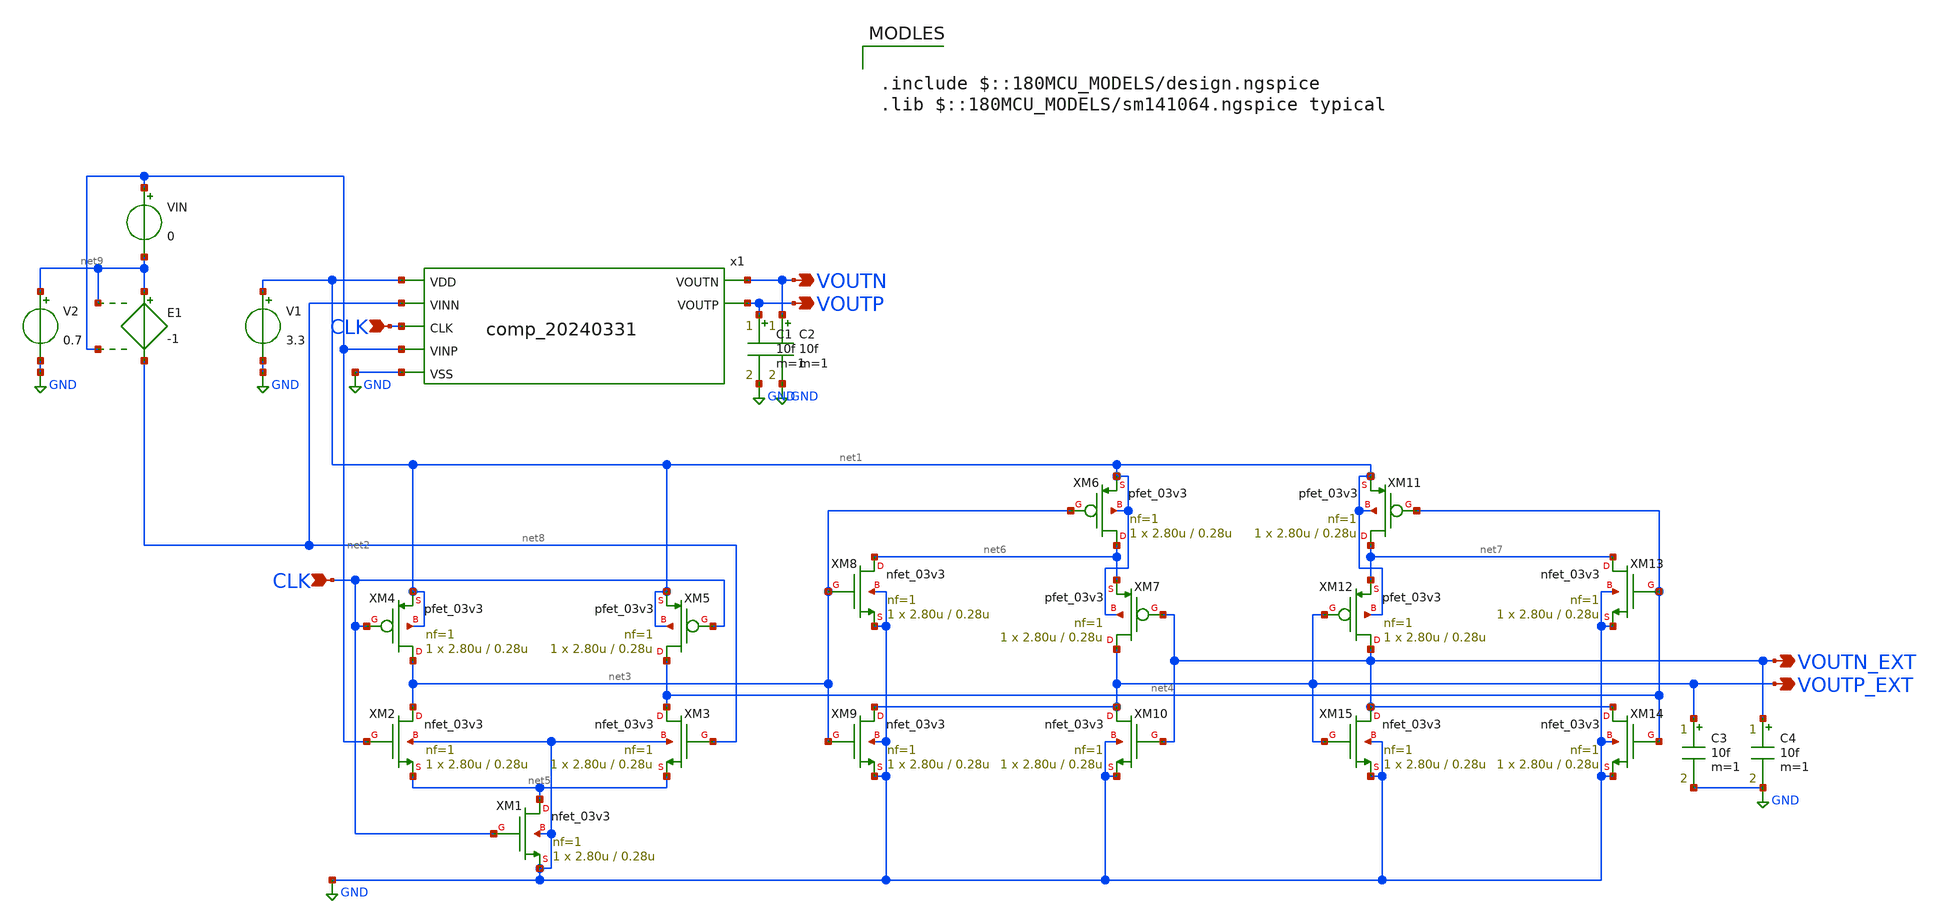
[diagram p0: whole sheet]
** sch_path: review/0407/comp_20240331/tb/tb_like_p78.sch
**.subckt tb_like_p78 CLK VOUTN VOUTP CLK VOUTP_EXT VOUTN_EXT
*.ipin CLK
*.opin VOUTN
*.opin VOUTP
*.ipin CLK
*.opin VOUTP_EXT
*.opin VOUTN_EXT
V1 net1 GND 3.3
V2 net9 GND 0.7
XM1 net5 CLK GND GND nfet_03v3 L=0.28u W=2.80u nf=1 ad='int((nf+1)/2) * W/nf * 0.18u' as='int((nf+2)/2) * W/nf * 0.18u'
+ pd='2*int((nf+1)/2) * (W/nf + 0.18u)' ps='2*int((nf+2)/2) * (W/nf + 0.18u)' nrd='0.18u / W' nrs='0.18u / W'
+ sa=0 sb=0 sd=0 m=1
XM2 net3 net2 net5 GND nfet_03v3 L=0.28u W=2.80u nf=1 ad='int((nf+1)/2) * W/nf * 0.18u' as='int((nf+2)/2) * W/nf * 0.18u'
+ pd='2*int((nf+1)/2) * (W/nf + 0.18u)' ps='2*int((nf+2)/2) * (W/nf + 0.18u)' nrd='0.18u / W' nrs='0.18u / W'
+ sa=0 sb=0 sd=0 m=1
XM4 net3 CLK net1 net1 pfet_03v3 L=0.28u W=2.80u nf=1 ad='int((nf+1)/2) * W/nf * 0.18u' as='int((nf+2)/2) * W/nf * 0.18u'
+ pd='2*int((nf+1)/2) * (W/nf + 0.18u)' ps='2*int((nf+2)/2) * (W/nf + 0.18u)' nrd='0.18u / W' nrs='0.18u / W'
+ sa=0 sb=0 sd=0 m=1
XM6 net6 net3 net1 net1 pfet_03v3 L=0.28u W=2.80u nf=1 ad='int((nf+1)/2) * W/nf * 0.18u' as='int((nf+2)/2) * W/nf * 0.18u'
+ pd='2*int((nf+1)/2) * (W/nf + 0.18u)' ps='2*int((nf+2)/2) * (W/nf + 0.18u)' nrd='0.18u / W' nrs='0.18u / W'
+ sa=0 sb=0 sd=0 m=1
XM7 VOUTP_EXT VOUTN_EXT net6 net1 pfet_03v3 L=0.28u W=2.80u nf=1 ad='int((nf+1)/2) * W/nf * 0.18u' as='int((nf+2)/2) * W/nf * 0.18u'
+ pd='2*int((nf+1)/2) * (W/nf + 0.18u)' ps='2*int((nf+2)/2) * (W/nf + 0.18u)' nrd='0.18u / W' nrs='0.18u / W'
+ sa=0 sb=0 sd=0 m=1
XM8 net6 net3 GND GND nfet_03v3 L=0.28u W=2.80u nf=1 ad='int((nf+1)/2) * W/nf * 0.18u' as='int((nf+2)/2) * W/nf * 0.18u'
+ pd='2*int((nf+1)/2) * (W/nf + 0.18u)' ps='2*int((nf+2)/2) * (W/nf + 0.18u)' nrd='0.18u / W' nrs='0.18u / W'
+ sa=0 sb=0 sd=0 m=1
XM9 VOUTP_EXT net3 GND GND nfet_03v3 L=0.28u W=2.80u nf=1 ad='int((nf+1)/2) * W/nf * 0.18u' as='int((nf+2)/2) * W/nf * 0.18u'
+ pd='2*int((nf+1)/2) * (W/nf + 0.18u)' ps='2*int((nf+2)/2) * (W/nf + 0.18u)' nrd='0.18u / W' nrs='0.18u / W'
+ sa=0 sb=0 sd=0 m=1
XM10 VOUTP_EXT VOUTN_EXT GND GND nfet_03v3 L=0.28u W=2.80u nf=1 ad='int((nf+1)/2) * W/nf * 0.18u' as='int((nf+2)/2) * W/nf * 0.18u'
+ pd='2*int((nf+1)/2) * (W/nf + 0.18u)' ps='2*int((nf+2)/2) * (W/nf + 0.18u)' nrd='0.18u / W' nrs='0.18u / W'
+ sa=0 sb=0 sd=0 m=1
XM3 net4 net8 net5 GND nfet_03v3 L=0.28u W=2.80u nf=1 ad='int((nf+1)/2) * W/nf * 0.18u' as='int((nf+2)/2) * W/nf * 0.18u'
+ pd='2*int((nf+1)/2) * (W/nf + 0.18u)' ps='2*int((nf+2)/2) * (W/nf + 0.18u)' nrd='0.18u / W' nrs='0.18u / W'
+ sa=0 sb=0 sd=0 m=1
XM5 net4 CLK net1 net1 pfet_03v3 L=0.28u W=2.80u nf=1 ad='int((nf+1)/2) * W/nf * 0.18u' as='int((nf+2)/2) * W/nf * 0.18u'
+ pd='2*int((nf+1)/2) * (W/nf + 0.18u)' ps='2*int((nf+2)/2) * (W/nf + 0.18u)' nrd='0.18u / W' nrs='0.18u / W'
+ sa=0 sb=0 sd=0 m=1
XM11 net7 net4 net1 net1 pfet_03v3 L=0.28u W=2.80u nf=1 ad='int((nf+1)/2) * W/nf * 0.18u' as='int((nf+2)/2) * W/nf * 0.18u'
+ pd='2*int((nf+1)/2) * (W/nf + 0.18u)' ps='2*int((nf+2)/2) * (W/nf + 0.18u)' nrd='0.18u / W' nrs='0.18u / W'
+ sa=0 sb=0 sd=0 m=1
XM12 VOUTN_EXT VOUTP_EXT net7 net1 pfet_03v3 L=0.28u W=2.80u nf=1 ad='int((nf+1)/2) * W/nf * 0.18u' as='int((nf+2)/2) * W/nf * 0.18u'
+ pd='2*int((nf+1)/2) * (W/nf + 0.18u)' ps='2*int((nf+2)/2) * (W/nf + 0.18u)' nrd='0.18u / W' nrs='0.18u / W'
+ sa=0 sb=0 sd=0 m=1
XM13 net7 net4 GND GND nfet_03v3 L=0.28u W=2.80u nf=1 ad='int((nf+1)/2) * W/nf * 0.18u' as='int((nf+2)/2) * W/nf * 0.18u'
+ pd='2*int((nf+1)/2) * (W/nf + 0.18u)' ps='2*int((nf+2)/2) * (W/nf + 0.18u)' nrd='0.18u / W' nrs='0.18u / W'
+ sa=0 sb=0 sd=0 m=1
XM14 VOUTN_EXT net4 GND GND nfet_03v3 L=0.28u W=2.80u nf=1 ad='int((nf+1)/2) * W/nf * 0.18u' as='int((nf+2)/2) * W/nf * 0.18u'
+ pd='2*int((nf+1)/2) * (W/nf + 0.18u)' ps='2*int((nf+2)/2) * (W/nf + 0.18u)' nrd='0.18u / W' nrs='0.18u / W'
+ sa=0 sb=0 sd=0 m=1
XM15 VOUTN_EXT VOUTP_EXT GND GND nfet_03v3 L=0.28u W=2.80u nf=1 ad='int((nf+1)/2) * W/nf * 0.18u' as='int((nf+2)/2) * W/nf * 0.18u'
+ pd='2*int((nf+1)/2) * (W/nf + 0.18u)' ps='2*int((nf+2)/2) * (W/nf + 0.18u)' nrd='0.18u / W' nrs='0.18u / W'
+ sa=0 sb=0 sd=0 m=1
x1 net2 VOUTP VOUTN net8 CLK net1 GND TOP
C1 VOUTP GND 10f m=1
C2 VOUTN GND 10f m=1
VIN net2 net9 0
E1 net9 net8 net9 net2 -1
C3 VOUTP_EXT GND 10f m=1
C4 VOUTN_EXT GND 10f m=1
**** begin user architecture code

.include $::180MCU_MODELS/design.ngspice
.lib $::180MCU_MODELS/sm141064.ngspice typical




VDD CLK 0 pulse (0 3.3 0 40p 40p 62.5n 125n) dc 0v
.include /media/tomoakitanaka/Documents/MyDocuments/personal/ISHIKAI/2024/Chipathon2023_ADC/gitefu/comp_20240331/TOP_pex_extracted.spice
.control
save all
let VSTART = 0
let VSTOP  = 10m
let VDELTA = 0.5m
let v_act   = 0
let i = 0;
while v_act < VSTOP
	tran 0.1n 40n
	alter VIN = v_act
	let v_act = v_act + VDELTA
	write result.raw
	set appendwrite
end
.endc



**** end user architecture code
**.ends
.GLOBAL GND
.end
